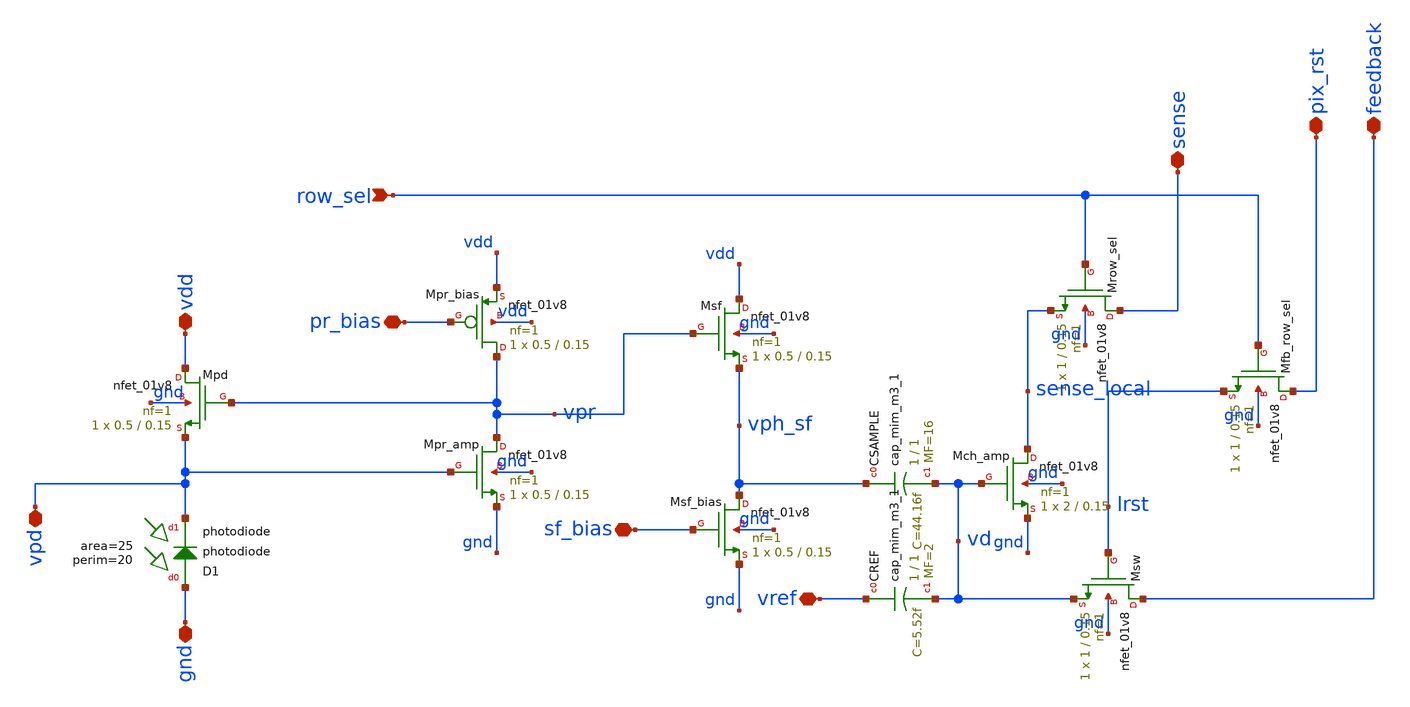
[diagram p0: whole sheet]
** sch_path: analog/klayout/production/final_merge_20260923/testbenches/cace/analog/xschem/openDVS_pixel_tia.sch
**.subckt openDVS_pixel_tia row_sel sense pix_rst feedback pr_bias vdd vref vpd sf_bias gnd
*.ipin row_sel
*.iopin sense
*.iopin pix_rst
*.iopin feedback
*.iopin pr_bias
*.iopin vdd
*.iopin vref
*.iopin vpd
*.iopin sf_bias
*.iopin gnd
XCSAMPLE vph_sf vd sky130_fd_pr__cap_mim_m3_1 W=1 L=1 MF=16 m=16
XCREF vref vd sky130_fd_pr__cap_mim_m3_1 W=1 L=1 MF=2 m=2
XMpd vdd vpr vpd gnd sky130_fd_pr__nfet_01v8 L=0.15 W=0.5 nf=1 ad='int((1 + 1)/2) * 0.5 / 1 * 0.29' as='int((1 + 2)/2) * 0.5 / 1 * 0.29'
+ pd='2*int((1 + 1)/2) * (0.5 / 1 + 0.29)' ps='2*int((1 + 2)/2) * (0.5 / 1 + 0.29)' nrd='0.29 / 0.5 ' nrs='0.29 / 0.5 '
+ sa=0 sb=0 sd=0 mult=1 m=1
XMch_amp sense_local vd gnd gnd sky130_fd_pr__nfet_01v8 L=0.15 W=2 nf=1 ad='int((1 + 1)/2) * 2 / 1 * 0.29'
+ as='int((1 + 2)/2) * 2 / 1 * 0.29' pd='2*int((1 + 1)/2) * (2 / 1 + 0.29)' ps='2*int((1 + 2)/2) * (2 / 1 + 0.29)'
+ nrd='0.29 / 2 ' nrs='0.29 / 2 ' sa=0 sb=0 sd=0 mult=1 m=1
XMsw feedback lrst vd gnd sky130_fd_pr__nfet_01v8 L=0.15 W=1 nf=1 ad='int((1 + 1)/2) * 1 / 1 * 0.29'
+ as='int((1 + 2)/2) * 1 / 1 * 0.29' pd='2*int((1 + 1)/2) * (1 / 1 + 0.29)' ps='2*int((1 + 2)/2) * (1 / 1 + 0.29)'
+ nrd='0.29 / 1 ' nrs='0.29 / 1 ' sa=0 sb=0 sd=0 mult=1 m=1
XMsf_bias vph_sf sf_bias gnd gnd sky130_fd_pr__nfet_01v8 L=0.15 W=0.5 nf=1 ad='int((1 + 1)/2) * 0.5 / 1 * 0.29'
+ as='int((1 + 2)/2) * 0.5 / 1 * 0.29' pd='2*int((1 + 1)/2) * (0.5 / 1 + 0.29)' ps='2*int((1 + 2)/2) * (0.5 / 1 + 0.29)'
+ nrd='0.29 / 0.5 ' nrs='0.29 / 0.5 ' sa=0 sb=0 sd=0 mult=1 m=1
XMsf vdd vpr vph_sf gnd sky130_fd_pr__nfet_01v8 L=0.15 W=0.5 nf=1 ad='int((1 + 1)/2) * 0.5 / 1 * 0.29'
+ as='int((1 + 2)/2) * 0.5 / 1 * 0.29' pd='2*int((1 + 1)/2) * (0.5 / 1 + 0.29)' ps='2*int((1 + 2)/2) * (0.5 / 1 + 0.29)'
+ nrd='0.29 / 0.5 ' nrs='0.29 / 0.5 ' sa=0 sb=0 sd=0 mult=1 m=1
XMrow_sel sense row_sel sense_local gnd sky130_fd_pr__nfet_01v8 L=0.15 W=1 nf=1 ad='int((1 + 1)/2) * 1 / 1 * 0.29'
+ as='int((1 + 2)/2) * 1 / 1 * 0.29' pd='2*int((1 + 1)/2) * (1 / 1 + 0.29)' ps='2*int((1 + 2)/2) * (1 / 1 + 0.29)'
+ nrd='0.29 / 1 ' nrs='0.29 / 1 ' sa=0 sb=0 sd=0 mult=1 m=1
XMfb_row_sel pix_rst row_sel lrst gnd sky130_fd_pr__nfet_01v8 L=0.15 W=1 nf=1 ad='int((1 + 1)/2) * 1 / 1 * 0.29'
+ as='int((1 + 2)/2) * 1 / 1 * 0.29' pd='2*int((1 + 1)/2) * (1 / 1 + 0.29)' ps='2*int((1 + 2)/2) * (1 / 1 + 0.29)'
+ nrd='0.29 / 1 ' nrs='0.29 / 1 ' sa=0 sb=0 sd=0 mult=1 m=1
XMpr_amp vpr vpd gnd gnd sky130_fd_pr__nfet_01v8 L=0.15 W=0.5 nf=1 ad='int((1 + 1)/2) * 0.5 / 1 * 0.29'
+ as='int((1 + 2)/2) * 0.5 / 1 * 0.29' pd='2*int((1 + 1)/2) * (0.5 / 1 + 0.29)' ps='2*int((1 + 2)/2) * (0.5 / 1 + 0.29)'
+ nrd='0.29 / 0.5 ' nrs='0.29 / 0.5 ' sa=0 sb=0 sd=0 mult=1 m=1
XMpr_bias vpr pr_bias vdd vdd sky130_fd_pr__nfet_01v8 L=0.15 W=0.5 nf=1 ad='int((1 + 1)/2) * 0.5 / 1 * 0.29'
+ as='int((1 + 2)/2) * 0.5 / 1 * 0.29' pd='2*int((1 + 1)/2) * (0.5 / 1 + 0.29)' ps='2*int((1 + 2)/2) * (0.5 / 1 + 0.29)'
+ nrd='0.29 / 0.5 ' nrs='0.29 / 0.5 ' sa=0 sb=0 sd=0 mult=1 m=1
XD1 gnd vpd sky130_fd_pr__photodiode area=25 perim=20
**.ends
.end
